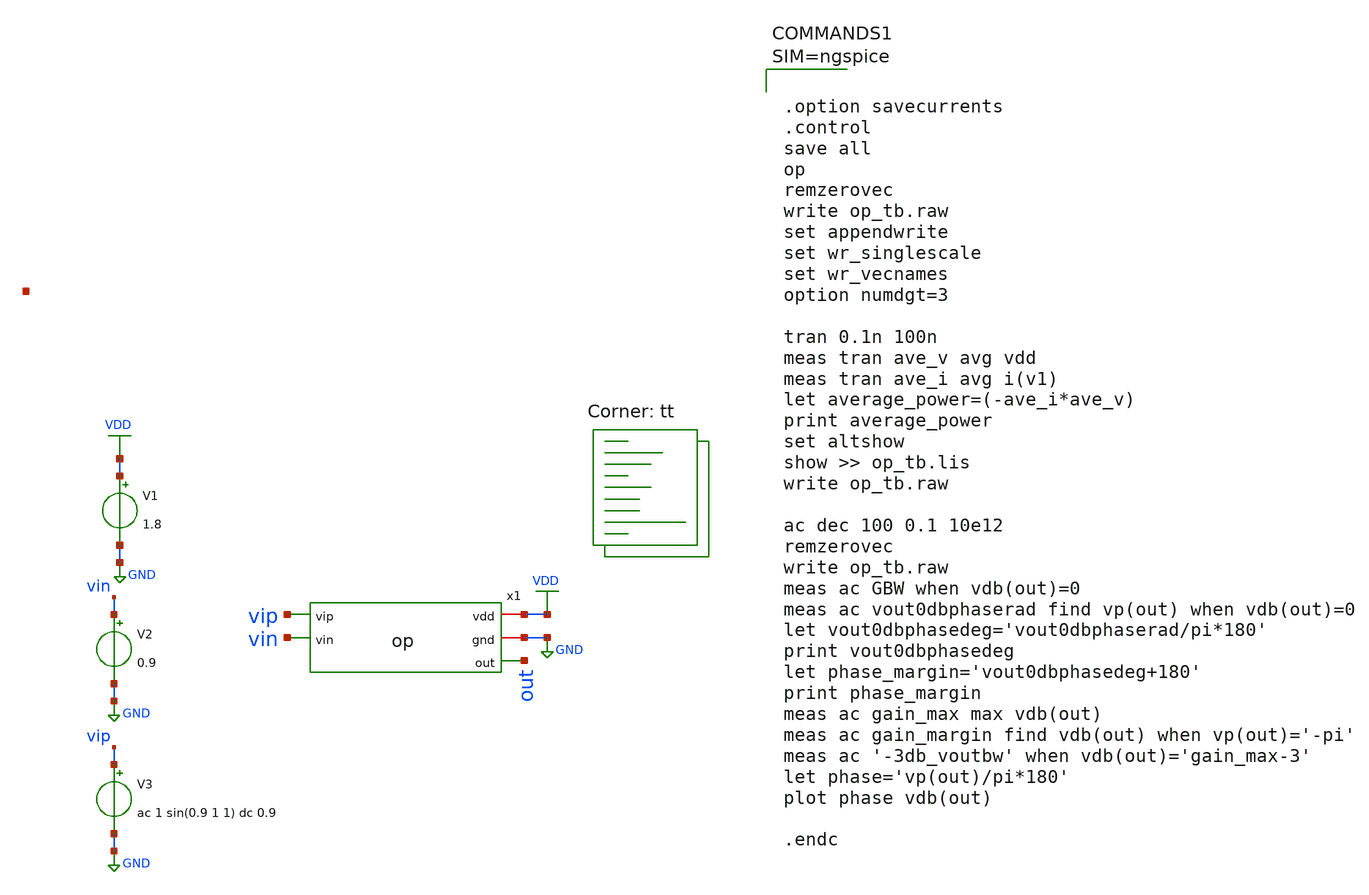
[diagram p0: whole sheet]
** sch_path: xschem/op_tb.sch
**.subckt op_tb
V1 VDD GND 1.8
V2 vin GND 0.9
V3 vip GND ac 1 sin(0.9 1 1) dc 0.9
x1 VDD GND vip vin out op
**** begin user architecture code



.option savecurrents
.control
save all
op
remzerovec
write op_tb.raw
set appendwrite
set wr_singlescale
set wr_vecnames
option numdgt=3

tran 0.1n 100n
meas tran ave_v avg vdd
meas tran ave_i avg i(v1)
let average_power=(-ave_i*ave_v)
print average_power
set altshow
show >> op_tb.lis
write op_tb.raw

ac dec 100 0.1 10e12
remzerovec
write op_tb.raw
meas ac GBW when vdb(out)=0
meas ac vout0dbphaserad find vp(out) when vdb(out)=0
let vout0dbphasedeg='vout0dbphaserad/pi*180'
print vout0dbphasedeg
let phase_margin='vout0dbphasedeg+180'
print phase_margin
meas ac gain_max max vdb(out)
meas ac gain_margin find vdb(out) when vp(out)='-pi'
meas ac '-3db_voutbw' when vdb(out)='gain_max-3'
let phase='vp(out)/pi*180'
plot phase vdb(out)

.endc



.lib $::SKYWATER_MODELS/sky130.lib.spice tt
**** end user architecture code
**.ends

* expanding   symbol:  op.sym # of pins=5
** sym_path: xschem/op.sym
** sch_path: xschem/op.sch
.subckt op vdd gnd vip vin out
*.iopin vdd
*.iopin gnd
*.ipin vip
*.ipin vin
*.opin out
.ends

.GLOBAL VDD
.GLOBAL GND
.end
